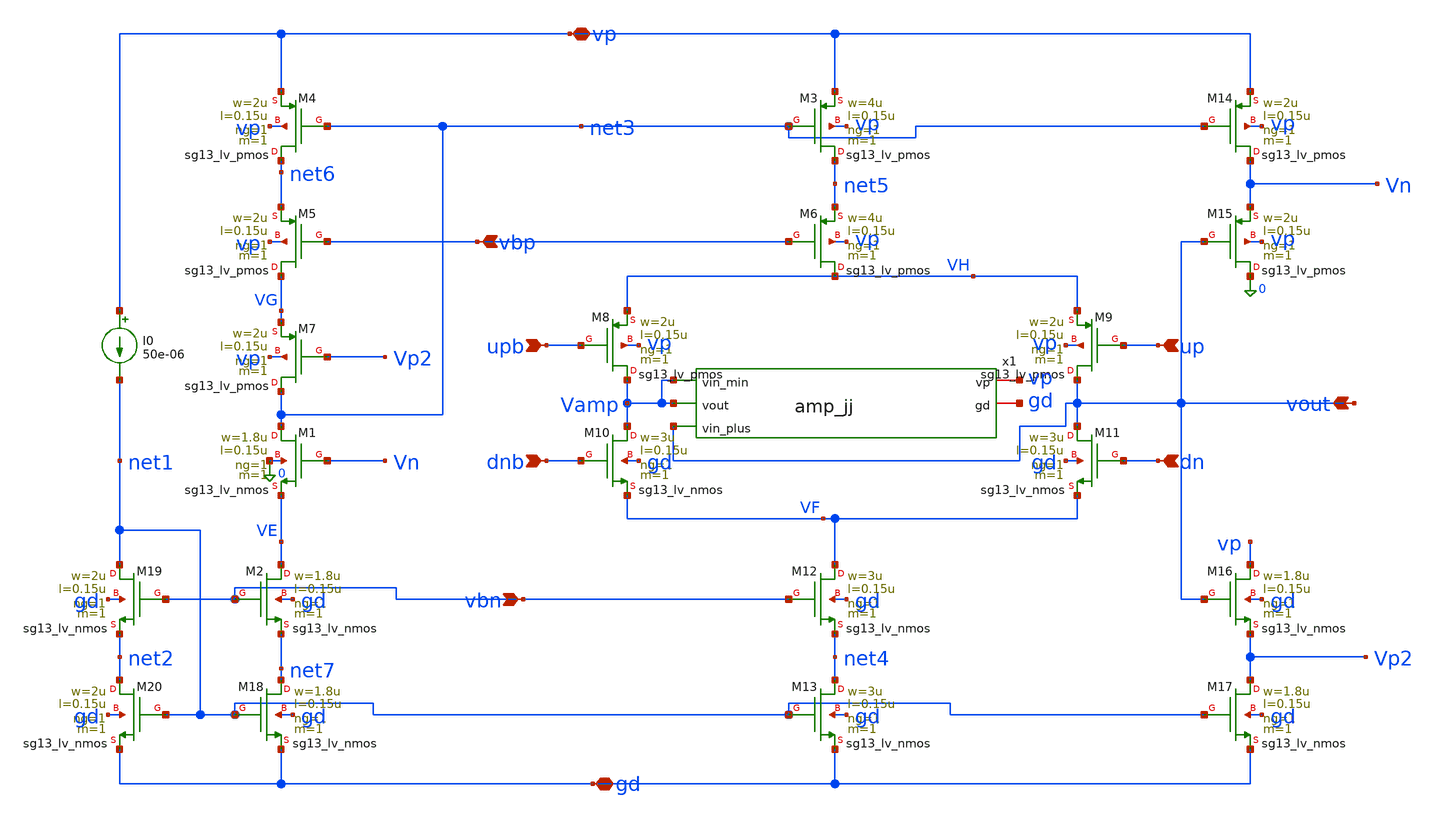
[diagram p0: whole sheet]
** sch_path: charge_pump/cp_v1.sch
**.subckt cp_v1 upb dnb up dn vp gd vout vbn vbp
*.ipin upb
*.ipin dnb
*.ipin up
*.ipin dn
*.iopin vp
*.iopin gd
*.opin vout
*.ipin vbn
*.ipin vbp
XM1 net3 Vn VE 0 sg13_lv_nmos w=1.8u l=0.15u ng=1 m=1 mm_ok=1
XM3 net5 net3 vp vp sg13_lv_pmos w=4u l=0.15u ng=1 m=1 mm_ok=1
XM4 net6 net3 vp vp sg13_lv_pmos w=2u l=0.15u ng=1 m=1 mm_ok=1
XM5 VG vbp net6 vp sg13_lv_pmos w=2u l=0.15u ng=1 m=1 mm_ok=1
XM6 VH vbp net5 vp sg13_lv_pmos w=4u l=0.15u ng=1 m=1 mm_ok=1
XM7 net3 Vp2 VG vp sg13_lv_pmos w=2u l=0.15u ng=1 m=1 mm_ok=1
XM8 Vamp upb VH vp sg13_lv_pmos w=2u l=0.15u ng=1 m=1 mm_ok=1
XM9 vout up VH vp sg13_lv_pmos w=2u l=0.15u ng=1 m=1 mm_ok=1
XM10 Vamp dnb VF gd sg13_lv_nmos w=3u l=0.15u ng=1 m=1 mm_ok=1
XM11 vout dn VF gd sg13_lv_nmos w=3u l=0.15u ng=1 m=1 mm_ok=1
XM12 VF vbn net4 gd sg13_lv_nmos w=3u l=0.15u ng=1 m=1 mm_ok=1
XM13 net4 net1 gd gd sg13_lv_nmos w=3u l=0.15u ng=1 m=1 mm_ok=1
XM14 Vn net3 vp vp sg13_lv_pmos w=2u l=0.15u ng=1 m=1 mm_ok=1
XM15 0 vout Vn vp sg13_lv_pmos w=2u l=0.15u ng=1 m=1 mm_ok=1
XM16 vp vout Vp2 gd sg13_lv_nmos w=1.8u l=0.15u ng=1 m=1 mm_ok=1
XM17 Vp2 net1 gd gd sg13_lv_nmos w=1.8u l=0.15u ng=1 m=1 mm_ok=1
XM2 VE vbn net7 gd sg13_lv_nmos w=1.8u l=0.15u ng=1 m=1 mm_ok=1
XM18 net7 net1 gd gd sg13_lv_nmos w=1.8u l=0.15u ng=1 m=1 mm_ok=1
XM19 net1 vbn net2 gd sg13_lv_nmos w=2u l=0.15u ng=1 m=1 mm_ok=1
XM20 net2 net1 gd gd sg13_lv_nmos w=2u l=0.15u ng=1 m=1 mm_ok=1
I0 vp net1 50e-06
x1 vp Vamp Vamp vout gd amp_jj
**.ends
.end
